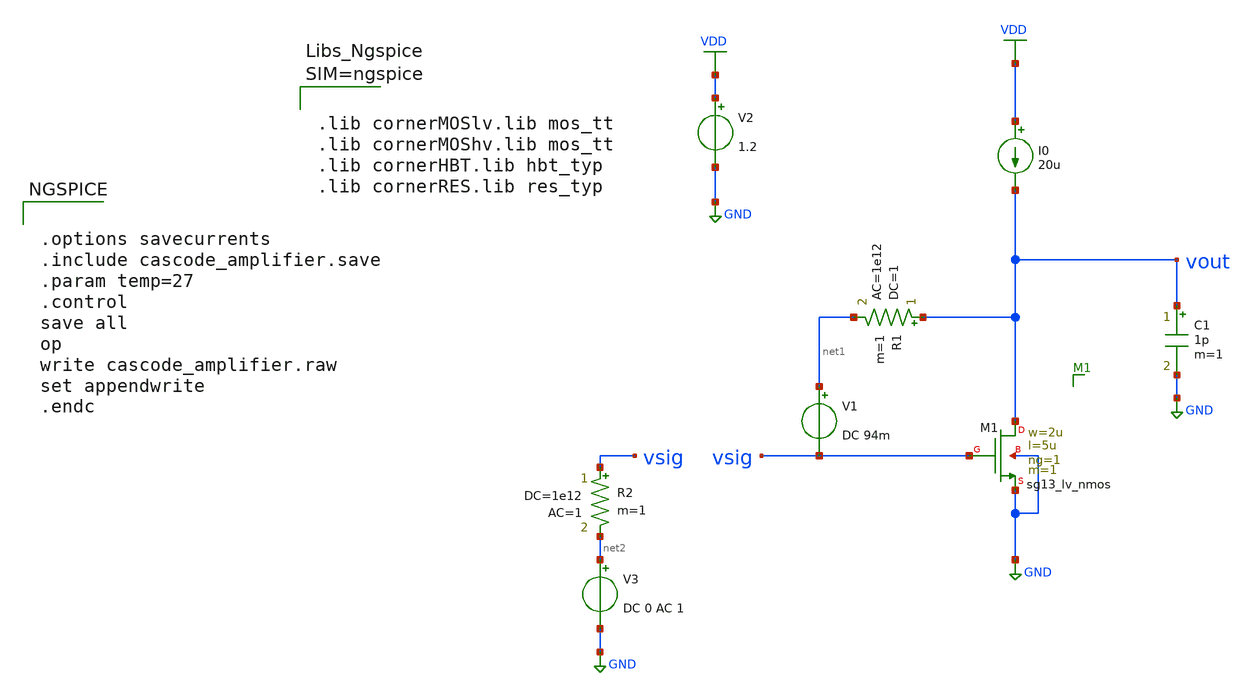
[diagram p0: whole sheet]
** sch_path: Schematics/cascode_amplifier.sch
**.subckt cascode_amplifier
XM1 vout vsig GND GND sg13_lv_nmos w=2u l=5u ng=1 m=1 mm_ok=1
V1 net1 vsig DC 94m
I0 VDD vout 20u
V2 VDD GND 1.2
C1 vout GND 1p m=1
V3 net2 GND DC 0 AC 1
R1 vout net1 1 ac=1e12 m=1
R2 vsig net2 1e12 ac=1 m=1
**** begin user architecture code



.lib cornerMOSlv.lib mos_tt
.lib cornerMOShv.lib mos_tt
.lib cornerHBT.lib hbt_typ
.lib cornerRES.lib res_typ





.options savecurrents
.include cascode_amplifier.save
.param temp=27
.control
save all
op
write cascode_amplifier.raw
set appendwrite
.endc


**** end user architecture code
**.ends
.GLOBAL GND
.GLOBAL VDD
.end
